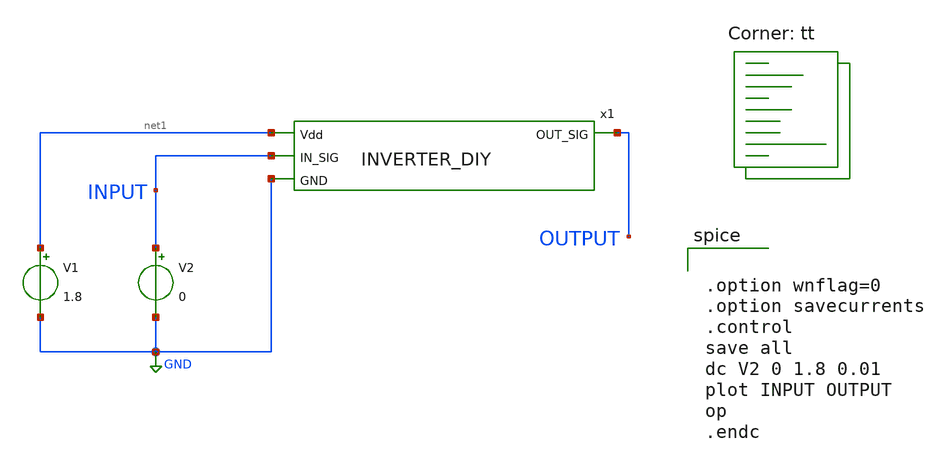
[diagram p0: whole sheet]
** sch_path: latihan_cmos/INVERTER_TB.sch
**.subckt INVERTER_TB
V1 net1 GND 1.8
V2 INPUT GND 0
x1 net1 INPUT OUTPUT GND INVERTER_DIY
**** begin user architecture code
.lib $::SKYWATER_MODELS/sky130.lib.spice tt


.option wnflag=0
.option savecurrents
.control
save all
dc V2 0 1.8 0.01
plot INPUT OUTPUT
op
.endc


**** end user architecture code
**.ends
.GLOBAL GND
.end
